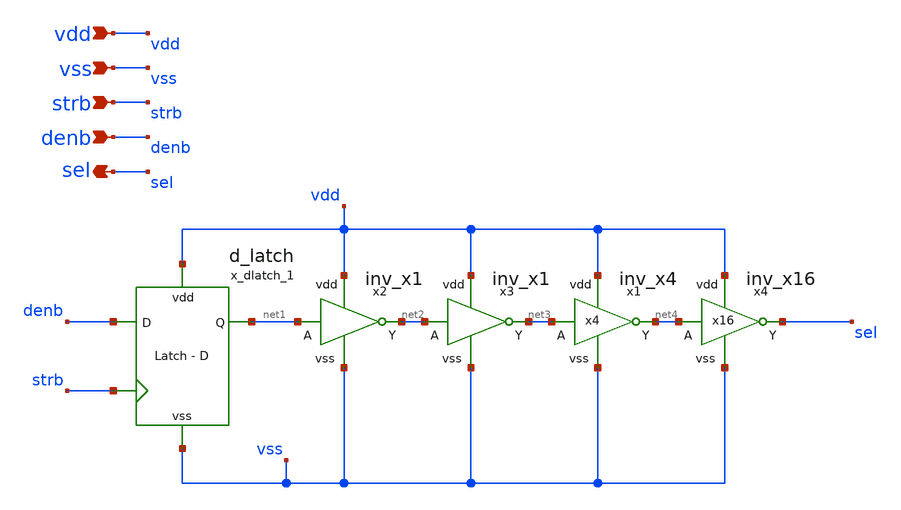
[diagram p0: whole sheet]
** sch_path: xschem/uc_latch/uc_latch.sch
**.subckt uc_latch strb vdd vss denb sel
*.ipin strb
*.ipin vdd
*.ipin vss
*.ipin denb
*.opin sel
x_dlatch_1 vdd vss strb denb net1 d_latch
x1 vdd net4 net3 vss inv_x4
x2 vdd net2 net1 vss inv_x1
x3 vdd net3 net2 vss inv_x1
x4 vdd sel net4 vss inv_x16
**.ends
.end
